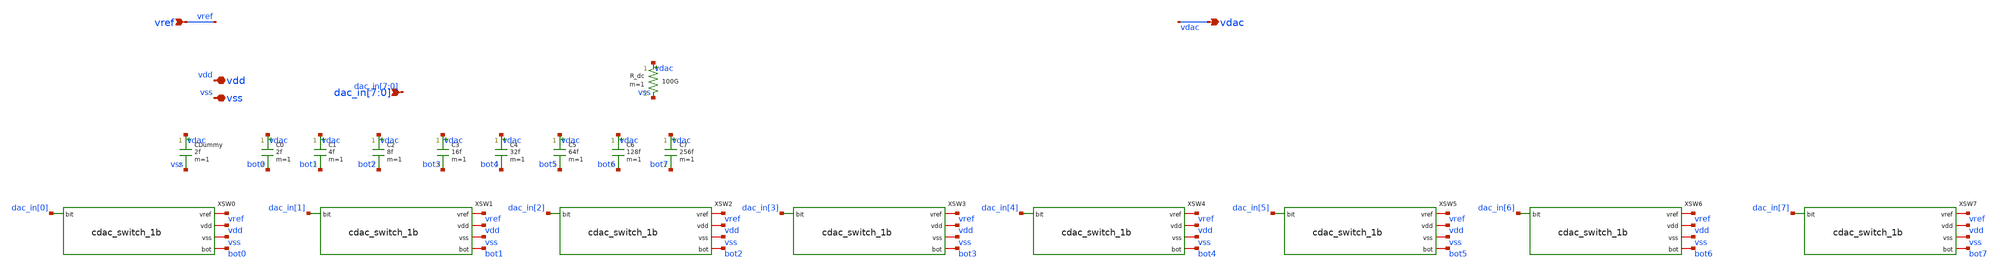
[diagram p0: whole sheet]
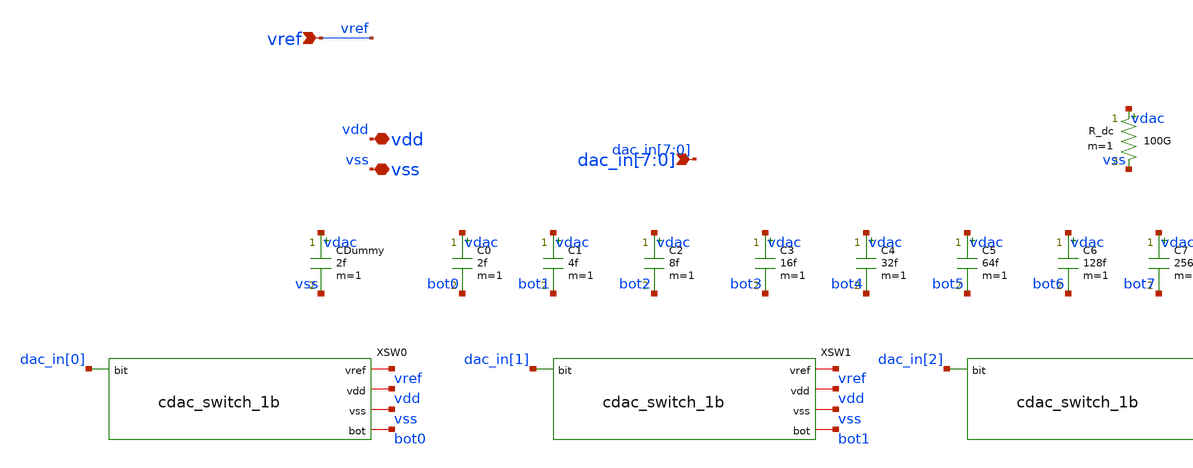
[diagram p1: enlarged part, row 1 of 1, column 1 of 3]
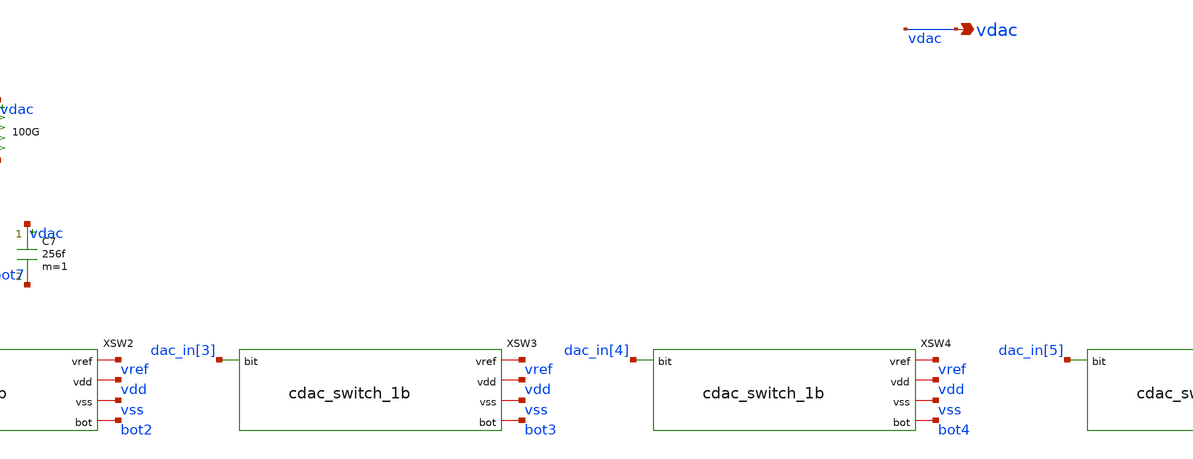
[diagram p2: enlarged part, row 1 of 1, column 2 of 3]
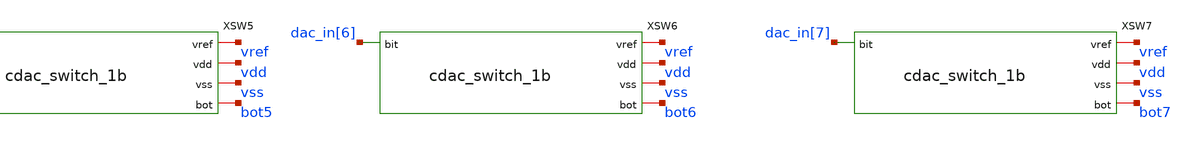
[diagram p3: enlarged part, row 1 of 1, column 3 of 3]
** sch_path: xschem/sar_adc/blocks/cdac/cdac_8bit.sch
**.subckt cdac_8bit vref vdd vss
*+ dac_in[7],dac_in[6],dac_in[5],dac_in[4],dac_in[3],dac_in[2],dac_in[1],dac_in[0] vdac
*.ipin vref
*.iopin vdd
*.iopin vss
*.ipin dac_in[7],dac_in[6],dac_in[5],dac_in[4],dac_in[3],dac_in[2],dac_in[1],dac_in[0]
*.opin vdac
XSW0 dac_in[0] vref vdd vss bot0 cdac_switch_1b
C0 vdac bot0 2f m=1
XSW1 dac_in[1] vref vdd vss bot1 cdac_switch_1b
C1 vdac bot1 4f m=1
XSW2 dac_in[2] vref vdd vss bot2 cdac_switch_1b
C2 vdac bot2 8f m=1
XSW3 dac_in[3] vref vdd vss bot3 cdac_switch_1b
C3 vdac bot3 16f m=1
XSW4 dac_in[4] vref vdd vss bot4 cdac_switch_1b
C4 vdac bot4 32f m=1
XSW5 dac_in[5] vref vdd vss bot5 cdac_switch_1b
C5 vdac bot5 64f m=1
XSW6 dac_in[6] vref vdd vss bot6 cdac_switch_1b
C6 vdac bot6 128f m=1
XSW7 dac_in[7] vref vdd vss bot7 cdac_switch_1b
C7 vdac bot7 256f m=1
CDummy vdac vss 2f m=1
R_dc vdac vss 100G m=1
**.ends

* expanding   symbol:  sar_adc/blocks/cdac/cdac_switch_1b.sym # of pins=5
** sym_path: xschem/sar_adc/blocks/cdac/cdac_switch_1b.sym
** sch_path: xschem/sar_adc/blocks/cdac/cdac_switch_1b.sch
.subckt cdac_switch_1b bit vref vdd vss bot
*.ipin bit
*.iopin vref
*.iopin vdd
*.iopin vss
*.iopin bot
XM1 bit_b bit vdd vdd pfet_03v3 L=0.28u W=4.0u nf=2 ad='int((nf+1)/2) * W/nf * 0.18u' as='int((nf+2)/2) * W/nf * 0.18u'
+ pd='2*int((nf+1)/2) * (W/nf + 0.18u)' ps='2*int((nf+2)/2) * (W/nf + 0.18u)' nrd='0.18u / W' nrs='0.18u / W'
+ sa=0 sb=0 sd=0 m=1
XM2 bit_b bit vss vss nfet_03v3 L=0.28u W=2.0u nf=2 ad='int((nf+1)/2) * W/nf * 0.18u' as='int((nf+2)/2) * W/nf * 0.18u'
+ pd='2*int((nf+1)/2) * (W/nf + 0.18u)' ps='2*int((nf+2)/2) * (W/nf + 0.18u)' nrd='0.18u / W' nrs='0.18u / W'
+ sa=0 sb=0 sd=0 m=1
XM3 bot bit_b vref vdd pfet_03v3 L=0.28u W=4.0u nf=2 ad='int((nf+1)/2) * W/nf * 0.18u' as='int((nf+2)/2) * W/nf * 0.18u'
+ pd='2*int((nf+1)/2) * (W/nf + 0.18u)' ps='2*int((nf+2)/2) * (W/nf + 0.18u)' nrd='0.18u / W' nrs='0.18u / W'
+ sa=0 sb=0 sd=0 m=1
XM4 bot bit vref vss nfet_03v3 L=0.28u W=2.0u nf=2 ad='int((nf+1)/2) * W/nf * 0.18u' as='int((nf+2)/2) * W/nf * 0.18u'
+ pd='2*int((nf+1)/2) * (W/nf + 0.18u)' ps='2*int((nf+2)/2) * (W/nf + 0.18u)' nrd='0.18u / W' nrs='0.18u / W'
+ sa=0 sb=0 sd=0 m=1
XM5 bot bit vss vdd pfet_03v3 L=0.28u W=4.0u nf=2 ad='int((nf+1)/2) * W/nf * 0.18u' as='int((nf+2)/2) * W/nf * 0.18u'
+ pd='2*int((nf+1)/2) * (W/nf + 0.18u)' ps='2*int((nf+2)/2) * (W/nf + 0.18u)' nrd='0.18u / W' nrs='0.18u / W'
+ sa=0 sb=0 sd=0 m=1
XM6 bot bit_b vss vss nfet_03v3 L=0.28u W=2.0u nf=2 ad='int((nf+1)/2) * W/nf * 0.18u' as='int((nf+2)/2) * W/nf * 0.18u'
+ pd='2*int((nf+1)/2) * (W/nf + 0.18u)' ps='2*int((nf+2)/2) * (W/nf + 0.18u)' nrd='0.18u / W' nrs='0.18u / W'
+ sa=0 sb=0 sd=0 m=1
.ends

.end
